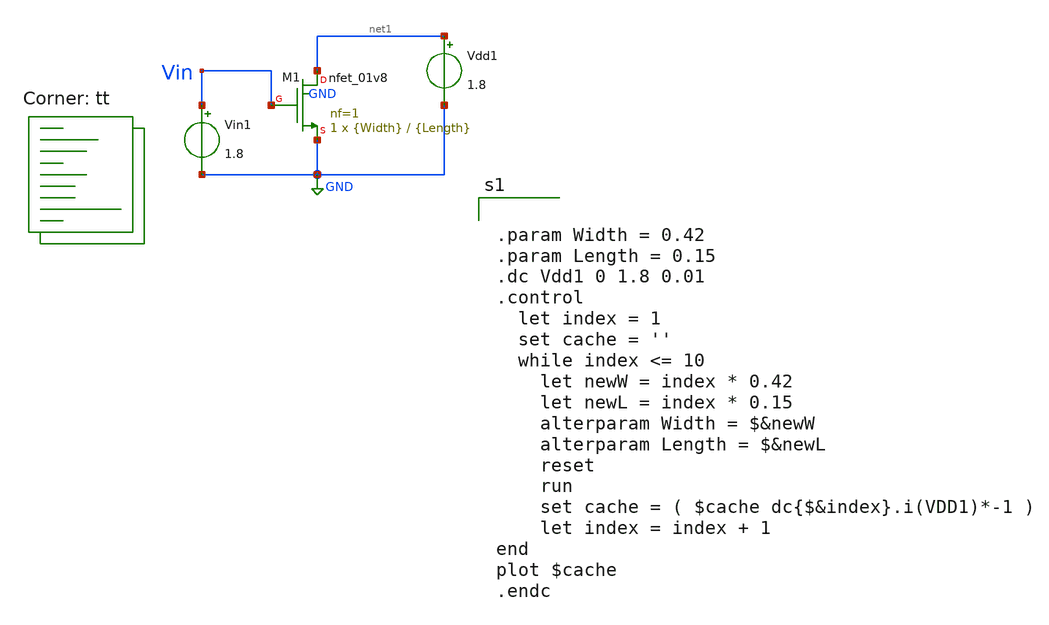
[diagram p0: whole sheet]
** sch_path: tut1/nmos/obsolete/tut1-expt3.sch
**.subckt tut1-expt3
Vin1 Vin GND 1.8
Vdd1 net1 GND 1.8
XM1 net1 Vin GND GND sky130_fd_pr__nfet_01v8 L={Length} W={Width} nf=1 ad='int((nf+1)/2) * W/nf * 0.29'
+ as='int((nf+2)/2) * W/nf * 0.29' pd='2*int((nf+1)/2) * (W/nf + 0.29)' ps='2*int((nf+2)/2) * (W/nf + 0.29)'
+ nrd='0.29 / W' nrs='0.29 / W' sa=0 sb=0 sd=0 mult=1 m=1
**** begin user architecture code
.lib $::SKYWATER_MODELS/sky130.lib.spice tt


.param Width = 0.42
.param Length = 0.15
.dc Vdd1 0 1.8 0.01
.control
  let index = 1
  set cache = ''
  while index <= 10
    let newW = index * 0.42
    let newL = index * 0.15
    alterparam Width = $&newW
    alterparam Length = $&newL
    reset
    run
    set cache = ( $cache dc{$&index}.i(VDD1)*-1 )
    let index = index + 1
end
plot $cache
.endc


**** end user architecture code
**.ends
.GLOBAL GND
.end
